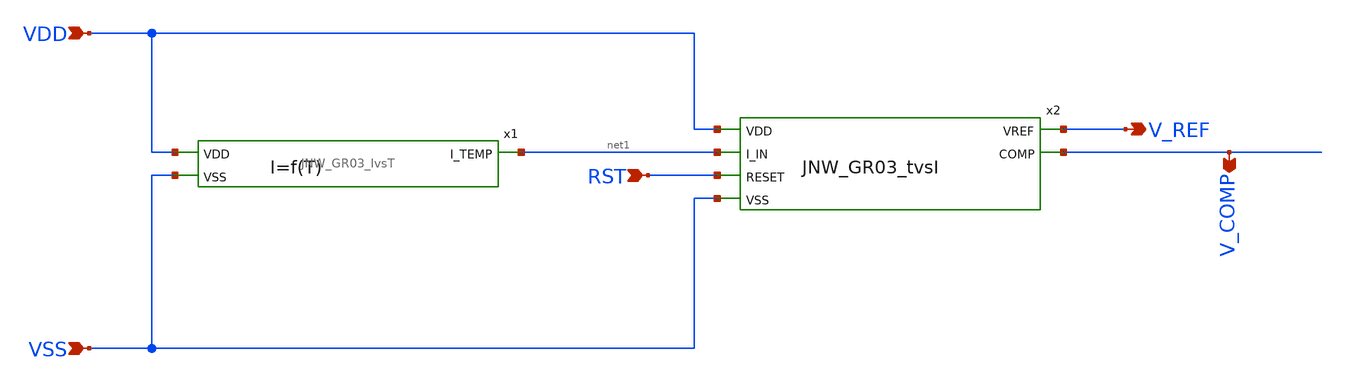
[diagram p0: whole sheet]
** sch_path: design/JNW_GR03_SKY130A/TB_JNW_GR03_ANALOG.sch
**.subckt TB_JNW_GR03_ANALOG VDD VSS V_COMP V_REF RST
*.ipin VDD
*.ipin VSS
*.opin V_COMP
*.opin V_REF
*.ipin RST
x1 VDD net1 VSS JNW_GR03_IvsT
x2 VDD net1 V_REF V_COMP RST VSS JNW_GR03_tvsI
**.ends
.end
